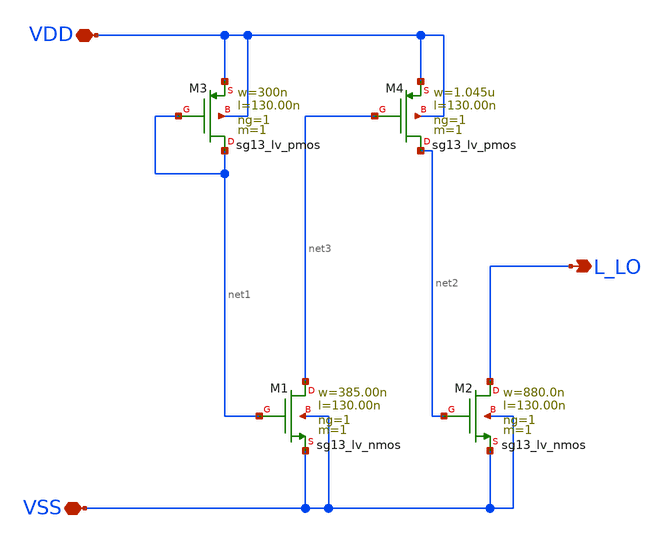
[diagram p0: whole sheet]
** sch_path: ihp-sg13g2/libs.tech/xschem/sg13g2_stdcells/sg13g2_tielo.sch
* Copyright 2023 IHP PDK Authors
* Licensed under the Apache License, Version 2.0 (the "License");
* you may not use this file except in compliance with the License.
* You may obtain a copy of the License at
* https://www.apache.org/licenses/LICENSE-2.0
* Unless required by applicable law or agreed to in writing, software
* distributed under the License is distributed on an "AS IS" BASIS,
* WITHOUT WARRANTIES OR CONDITIONS OF ANY KIND, either express or implied.
* See the License for the specific language governing permissions and
* limitations under the License.
**.subckt sg13g2_tielo L_LO VDD VSS
*.opin L_LO
*.iopin VDD
*.iopin VSS
XM1 net3 net1 VSS VSS sg13_lv_nmos w=385.00n l=130.00n ng=1 m=1 mm_ok=1
XM2 L_LO net2 VSS VSS sg13_lv_nmos w=880.0n l=130.00n ng=1 m=1 mm_ok=1
XM3 net1 net1 VDD VDD sg13_lv_pmos w=300n l=130.00n ng=1 m=1 mm_ok=1
XM4 net2 net3 VDD VDD sg13_lv_pmos w=1.045u l=130.00n ng=1 m=1 mm_ok=1
**.ends
.end
